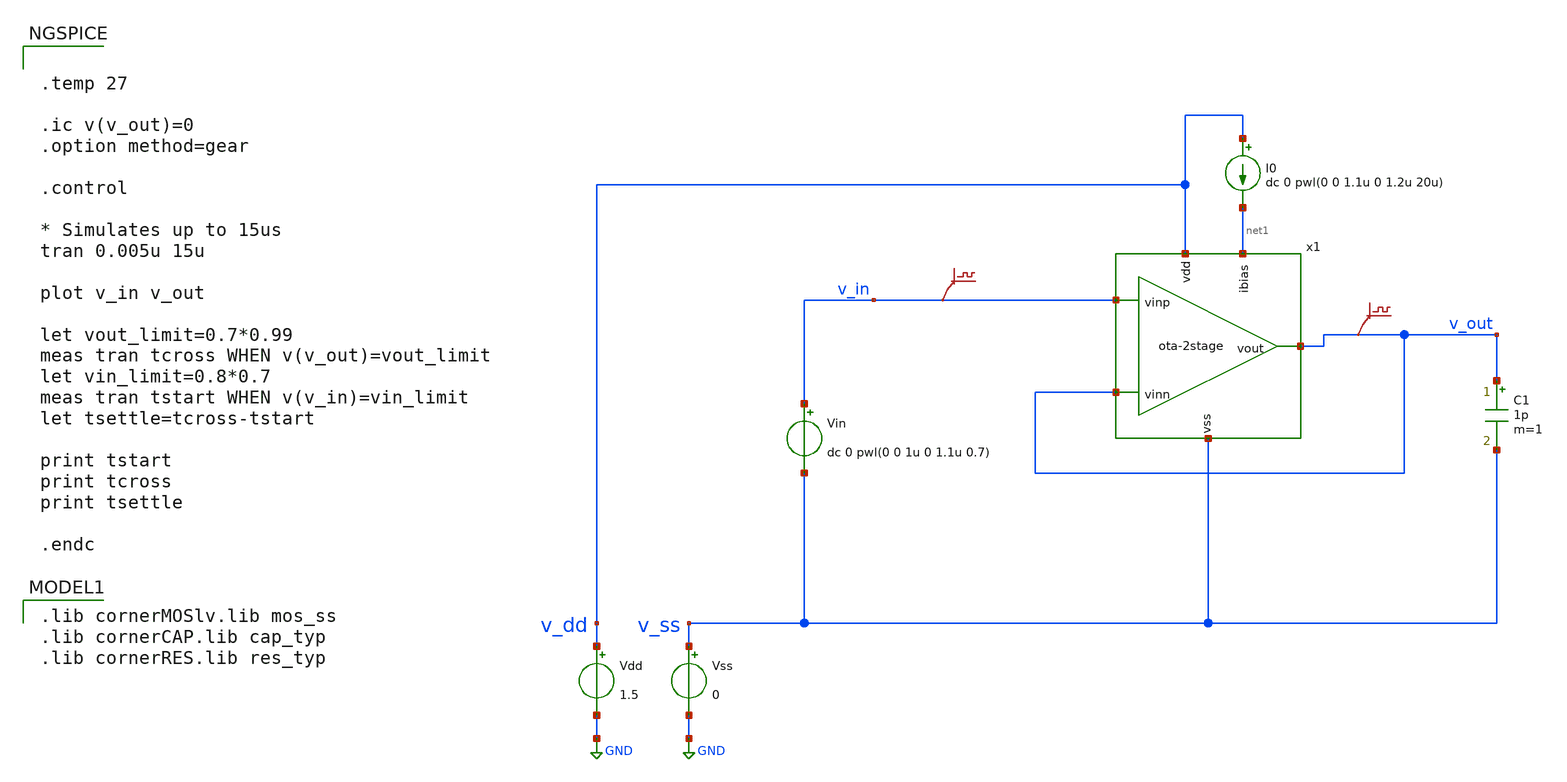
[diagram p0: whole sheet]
** sch_path: xschem/ota-2stage_tb-tran.sch
**.subckt ota-2stage_tb-tran
Vdd v_dd GND 1.5
Vss v_ss GND 0
C1 v_out v_ss 1p m=1
Vin v_in v_ss dc 0 pwl(0 0 1u 0 1.1u 0.7)
I0 v_dd net1 dc 0 pwl(0 0 1.1u 0 1.2u 20u)
.save v(v_in)
.save v(v_out)
x1 v_dd net1 v_out v_out v_in v_ss ota-2stage
**** begin user architecture code
 .lib cornerMOSlv.lib mos_ss
.lib cornerCAP.lib cap_typ
.lib cornerRES.lib res_typ



.temp 27

.ic v(v_out)=0
.option method=gear

.control

* Simulates up to 15us
tran 0.005u 15u

plot v_in v_out

let vout_limit=0.7*0.99
meas tran tcross WHEN v(v_out)=vout_limit
let vin_limit=0.8*0.7
meas tran tstart WHEN v(v_in)=vin_limit
let tsettle=tcross-tstart

print tstart
print tcross
print tsettle

.endc


**** end user architecture code
**.ends
.GLOBAL GND
.end
